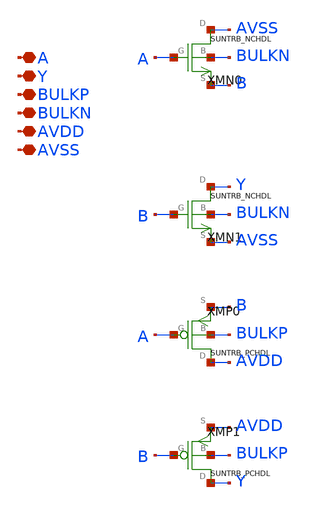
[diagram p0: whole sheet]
** sch_path: ip/sun_trb_sky130nm/design/SUN_TRB_SKY130NM/SUNTRB_BFX1_CV.sch
**.subckt SUNTRB_BFX1_CV A Y BULKP BULKN AVDD AVSS
*.iopin A
*.iopin Y
*.iopin BULKP
*.iopin BULKN
*.iopin AVDD
*.iopin AVSS
XMN0 AVSS A B BULKN SUNTRB_NCHDL xoffset=0 yoffset=0 angle=0
XMN1 Y B AVSS BULKN SUNTRB_NCHDL xoffset=0 yoffset=0 angle=0
XMP0 AVDD A B BULKP SUNTRB_PCHDL xoffset=0 yoffset=0 angle=0
XMP1 Y B AVDD BULKP SUNTRB_PCHDL xoffset=0 yoffset=0 angle=0
**.ends
.end
